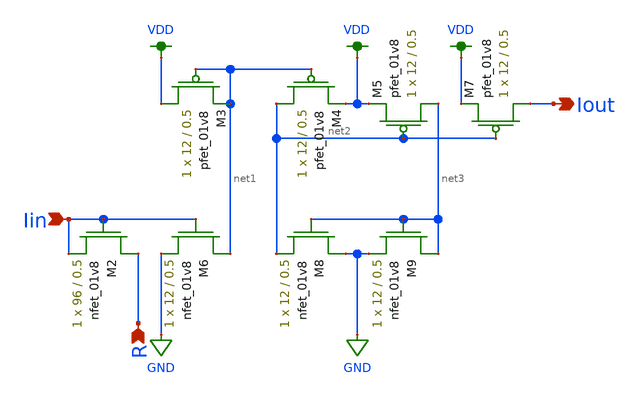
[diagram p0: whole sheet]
** sch_path: modules/current_mirror.sch
**.subckt current_mirror R Iout Iin
*.ipin R
*.opin Iout
*.ipin Iin
XM2 R Iin Iin GND sky130_fd_pr__nfet_01v8 L=0.5 W=96 nf=1 ad='int((nf+1)/2) * W/nf * 0.29' as='int((nf+2)/2) * W/nf * 0.29'
+ pd='2*int((nf+1)/2) * (W/nf + 0.29)' ps='2*int((nf+2)/2) * (W/nf + 0.29)' nrd='0.29 / W' nrs='0.29 / W'
+ sa=0 sb=0 sd=0 mult=1 m=1
XM3 VDD net1 net1 VDD sky130_fd_pr__pfet_01v8 L=0.5 W=12 nf=1 ad='int((nf+1)/2) * W/nf * 0.29' as='int((nf+2)/2) * W/nf * 0.29'
+ pd='2*int((nf+1)/2) * (W/nf + 0.29)' ps='2*int((nf+2)/2) * (W/nf + 0.29)' nrd='0.29 / W' nrs='0.29 / W'
+ sa=0 sb=0 sd=0 mult=1 m=1
XM4 net2 net1 VDD VDD sky130_fd_pr__pfet_01v8 L=0.5 W=12 nf=1 ad='int((nf+1)/2) * W/nf * 0.29' as='int((nf+2)/2) * W/nf * 0.29'
+ pd='2*int((nf+1)/2) * (W/nf + 0.29)' ps='2*int((nf+2)/2) * (W/nf + 0.29)' nrd='0.29 / W' nrs='0.29 / W'
+ sa=0 sb=0 sd=0 mult=1 m=1
XM5 net3 net2 VDD VDD sky130_fd_pr__pfet_01v8 L=0.5 W=12 nf=1 ad='int((nf+1)/2) * W/nf * 0.29' as='int((nf+2)/2) * W/nf * 0.29'
+ pd='2*int((nf+1)/2) * (W/nf + 0.29)' ps='2*int((nf+2)/2) * (W/nf + 0.29)' nrd='0.29 / W' nrs='0.29 / W'
+ sa=0 sb=0 sd=0 mult=1 m=1
XM7 Iout net2 VDD VDD sky130_fd_pr__pfet_01v8 L=0.5 W=12 nf=1 ad='int((nf+1)/2) * W/nf * 0.29' as='int((nf+2)/2) * W/nf * 0.29'
+ pd='2*int((nf+1)/2) * (W/nf + 0.29)' ps='2*int((nf+2)/2) * (W/nf + 0.29)' nrd='0.29 / W' nrs='0.29 / W'
+ sa=0 sb=0 sd=0 mult=1 m=1
XM6 net1 Iin GND GND sky130_fd_pr__nfet_01v8 L=0.5 W=12 nf=1 ad='int((nf+1)/2) * W/nf * 0.29' as='int((nf+2)/2) * W/nf * 0.29'
+ pd='2*int((nf+1)/2) * (W/nf + 0.29)' ps='2*int((nf+2)/2) * (W/nf + 0.29)' nrd='0.29 / W' nrs='0.29 / W'
+ sa=0 sb=0 sd=0 mult=1 m=1
XM8 GND net3 net2 GND sky130_fd_pr__nfet_01v8 L=0.5 W=12 nf=1 ad='int((nf+1)/2) * W/nf * 0.29' as='int((nf+2)/2) * W/nf * 0.29'
+ pd='2*int((nf+1)/2) * (W/nf + 0.29)' ps='2*int((nf+2)/2) * (W/nf + 0.29)' nrd='0.29 / W' nrs='0.29 / W'
+ sa=0 sb=0 sd=0 mult=1 m=1
XM9 net3 net3 GND GND sky130_fd_pr__nfet_01v8 L=0.5 W=12 nf=1 ad='int((nf+1)/2) * W/nf * 0.29' as='int((nf+2)/2) * W/nf * 0.29'
+ pd='2*int((nf+1)/2) * (W/nf + 0.29)' ps='2*int((nf+2)/2) * (W/nf + 0.29)' nrd='0.29 / W' nrs='0.29 / W'
+ sa=0 sb=0 sd=0 mult=1 m=1
**.ends
.GLOBAL VDD
.GLOBAL GND
.end
